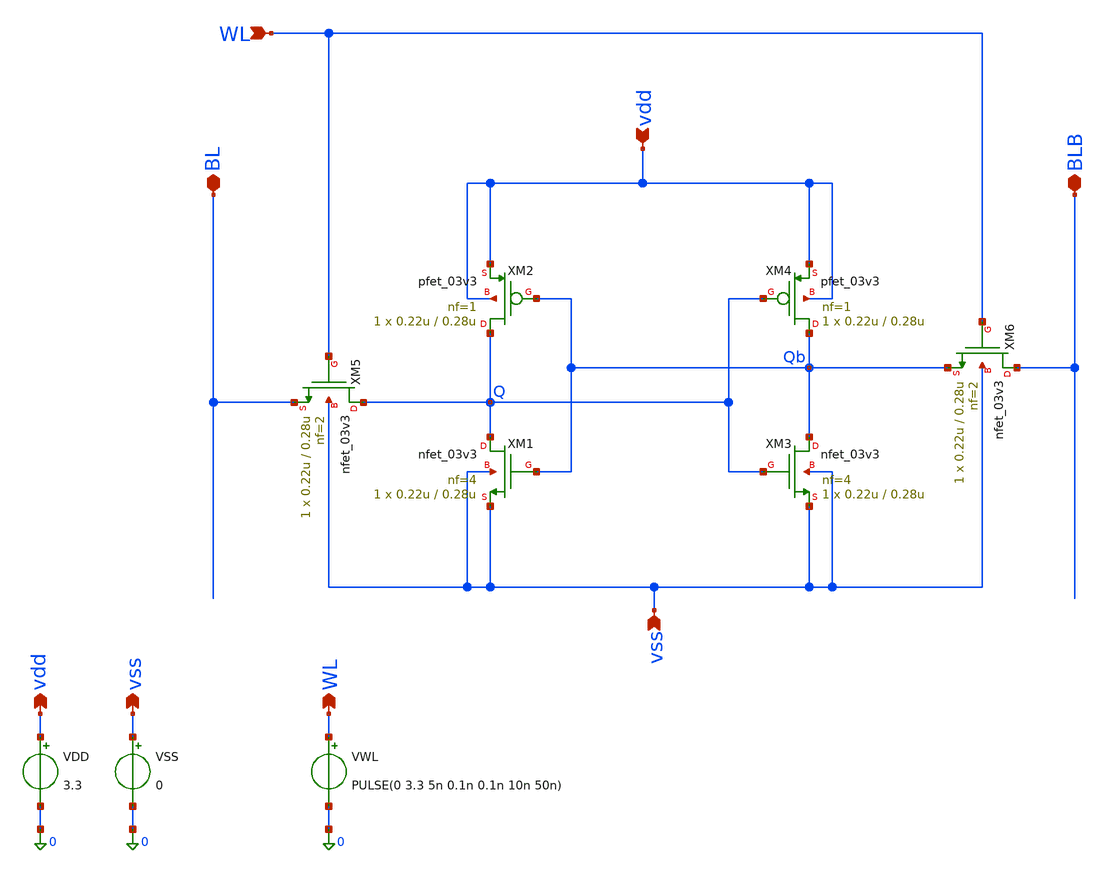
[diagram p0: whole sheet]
** sch_path: src/analog/6T_sram_03v3.sch
**.subckt 6T_sram_03v3 vdd vss BLB BL WL vdd vss WL
*.ipin vdd
*.ipin vss
*.iopin BLB
*.iopin BL
*.ipin WL
*.opin vdd
*.opin vss
*.opin WL
XM1 Q Qb vss vss nfet_03v3 L=0.28u W=0.22u nf=4 ad='int((nf+1)/2) * W/nf * 0.18u' as='int((nf+2)/2) * W/nf * 0.18u'
+ pd='2*int((nf+1)/2) * (W/nf + 0.18u)' ps='2*int((nf+2)/2) * (W/nf + 0.18u)' nrd='0.18u / W' nrs='0.18u / W'
+ sa=0 sb=0 sd=0 m=1
XM2 Q Qb vdd vdd pfet_03v3 L=0.28u W=0.22u nf=1 ad='int((nf+1)/2) * W/nf * 0.18u' as='int((nf+2)/2) * W/nf * 0.18u'
+ pd='2*int((nf+1)/2) * (W/nf + 0.18u)' ps='2*int((nf+2)/2) * (W/nf + 0.18u)' nrd='0.18u / W' nrs='0.18u / W'
+ sa=0 sb=0 sd=0 m=1
XM3 Qb Q vss vss nfet_03v3 L=0.28u W=0.22u nf=4 ad='int((nf+1)/2) * W/nf * 0.18u' as='int((nf+2)/2) * W/nf * 0.18u'
+ pd='2*int((nf+1)/2) * (W/nf + 0.18u)' ps='2*int((nf+2)/2) * (W/nf + 0.18u)' nrd='0.18u / W' nrs='0.18u / W'
+ sa=0 sb=0 sd=0 m=1
XM4 Qb Q vdd vdd pfet_03v3 L=0.28u W=0.22u nf=1 ad='int((nf+1)/2) * W/nf * 0.18u' as='int((nf+2)/2) * W/nf * 0.18u'
+ pd='2*int((nf+1)/2) * (W/nf + 0.18u)' ps='2*int((nf+2)/2) * (W/nf + 0.18u)' nrd='0.18u / W' nrs='0.18u / W'
+ sa=0 sb=0 sd=0 m=1
XM5 Q WL BL vss nfet_03v3 L=0.28u W=0.22u nf=2 ad='int((nf+1)/2) * W/nf * 0.18u' as='int((nf+2)/2) * W/nf * 0.18u'
+ pd='2*int((nf+1)/2) * (W/nf + 0.18u)' ps='2*int((nf+2)/2) * (W/nf + 0.18u)' nrd='0.18u / W' nrs='0.18u / W'
+ sa=0 sb=0 sd=0 m=1
XM6 BLB WL Qb vss nfet_03v3 L=0.28u W=0.22u nf=2 ad='int((nf+1)/2) * W/nf * 0.18u' as='int((nf+2)/2) * W/nf * 0.18u'
+ pd='2*int((nf+1)/2) * (W/nf + 0.18u)' ps='2*int((nf+2)/2) * (W/nf + 0.18u)' nrd='0.18u / W' nrs='0.18u / W'
+ sa=0 sb=0 sd=0 m=1
VDD vdd 0 3.3
VSS vss 0 0
VWL WL 0 PULSE(0 3.3 5n 0.1n 0.1n 10n 50n)
**** begin user architecture code

.include $::180MCU_MODELS/design.ngspice
.lib $::180MCU_MODELS/sm141064.ngspice typical




** Initial Conditions -- Set BL to '1' and BLB to '0'
.ic v(Q)=0 v(Qb)=3.3 v(BL)=3.3 v(BLB)=0

.control
save all

** Define Write Line Pulse signal
let fsig_w = 100M
let tper_w = 1/fsig_w
let tfr_w = 0.01*tper_w
let ton_w = 0.5*tper_w-2*tfr_w

** Transient analysis
tran 0.01n 50n uic

** Plot the waveforms
plot q qb wl
plot bl blb wl

write 6t_sram_03v3_tb.raw
.endc



**** end user architecture code
**.ends
.end
